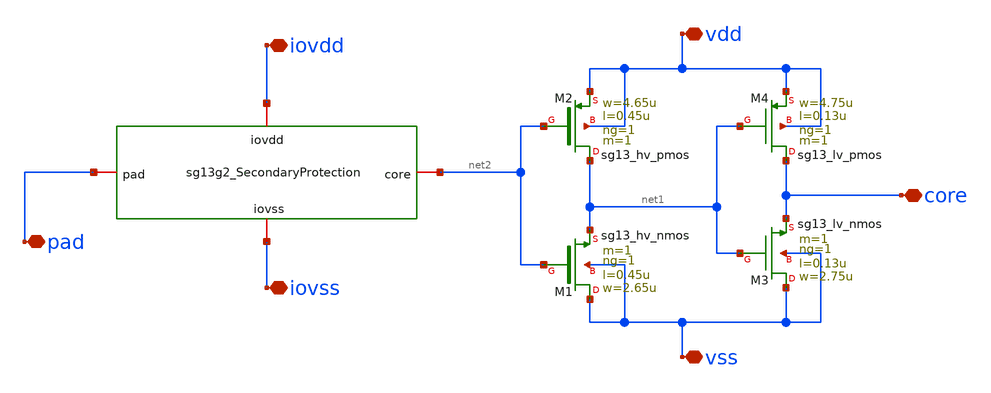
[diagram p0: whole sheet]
** sch_path: ihp-sg13g2/libs.ref/sg13g2_io/xschem/sg13g2_LevelDown.sch
**.subckt sg13g2_LevelDown vdd vss iovdd iovss pad core
*.iopin vdd
*.iopin vss
*.iopin iovdd
*.iopin iovss
*.iopin pad
*.iopin core
XM1 vss net2 net1 vss sg13_hv_nmos w=2.65u l=0.45u ng=1 m=1 mm_ok=1
XM2 net1 net2 vdd vdd sg13_hv_pmos w=4.65u l=0.45u ng=1 m=1 mm_ok=1
XM3 vss net1 core vss sg13_lv_nmos w=2.75u l=0.13u ng=1 m=1 mm_ok=1
XM4 core net1 vdd vdd sg13_lv_pmos w=4.75u l=0.13u ng=1 m=1 mm_ok=1
x1 iovdd pad net2 iovss sg13g2_SecondaryProtection
**.ends

* expanding   symbol:  sg13g2_SecondaryProtection.sym # of pins=4
** sym_path: ihp-sg13g2/libs.ref/sg13g2_io/xschem/sg13g2_SecondaryProtection.sym
** sch_path: ihp-sg13g2/libs.ref/sg13g2_io/xschem/sg13g2_SecondaryProtection.sch
.subckt sg13g2_SecondaryProtection iovdd pad core iovss
*.iopin iovdd
*.iopin iovss
*.iopin core
*.iopin pad
XR1 core pad sub! rppd w=1e-6 l=2e-6 m=1 b=0 mm_ok=1
XD1 iovss core dantenna l=3.1u w=0.64u
XD2 core iovdd dpantenna l=0.64u w=4.98u
.ends

.end
